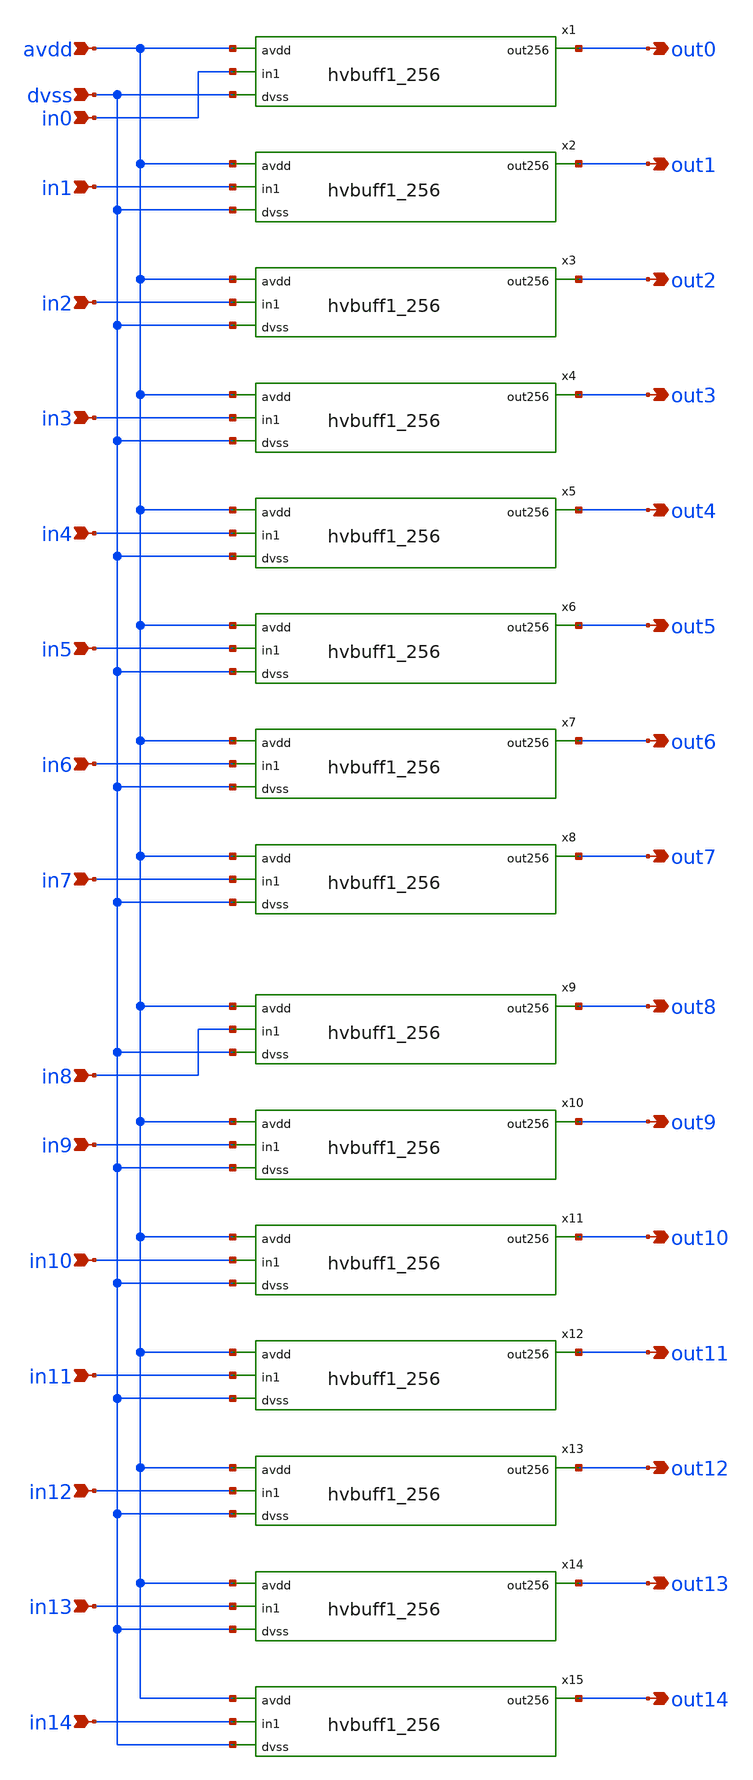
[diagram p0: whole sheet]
** sch_path: xschem/buff15ch.sch
**.subckt buff15ch out0 out1 out2 out3 out4 out5 out6 out7 in0 in1 in2 in3 in4 in5 in6 in7 out8 out9
*+ out10 out11 out12 out13 out14 in8 in9 in10 in11 in12 in13 in14 avdd dvss
*.opin out0
*.opin out1
*.opin out2
*.opin out3
*.opin out4
*.opin out5
*.opin out6
*.opin out7
*.ipin in0
*.ipin in1
*.ipin in2
*.ipin in3
*.ipin in4
*.ipin in5
*.ipin in6
*.ipin in7
*.opin out8
*.opin out9
*.opin out10
*.opin out11
*.opin out12
*.opin out13
*.opin out14
*.ipin in8
*.ipin in9
*.ipin in10
*.ipin in11
*.ipin in12
*.ipin in13
*.ipin in14
*.ipin avdd
*.ipin dvss
x1 avdd in0 out0 dvss hvbuff1_256
x2 avdd in1 out1 dvss hvbuff1_256
x3 avdd in2 out2 dvss hvbuff1_256
x4 avdd in3 out3 dvss hvbuff1_256
x5 avdd in4 out4 dvss hvbuff1_256
x6 avdd in5 out5 dvss hvbuff1_256
x7 avdd in6 out6 dvss hvbuff1_256
x8 avdd in7 out7 dvss hvbuff1_256
x9 avdd in8 out8 dvss hvbuff1_256
x10 avdd in9 out9 dvss hvbuff1_256
x11 avdd in10 out10 dvss hvbuff1_256
x12 avdd in11 out11 dvss hvbuff1_256
x13 avdd in12 out12 dvss hvbuff1_256
x14 avdd in13 out13 dvss hvbuff1_256
x15 avdd in14 out14 dvss hvbuff1_256
**.ends

* expanding   symbol:  hvbuff1_256.sym # of pins=4
** sym_path: xschem/hvbuff1_256.sym
** sch_path: xschem/hvbuff1_256.sch
.subckt hvbuff1_256 avdd in1 out256 dvss
*.ipin avdd
*.ipin in1
*.ipin dvss
*.opin out256
x2 net1 dvss dvss avdd avdd net2 sky130_fd_sc_hvl__inv_4
x1 net2 dvss dvss avdd avdd net3 sky130_fd_sc_hvl__inv_16
x3 net3 dvss dvss avdd avdd out256 sky130_fd_sc_hvl__inv_16
x4 net3 dvss dvss avdd avdd out256 sky130_fd_sc_hvl__inv_16
x5 net3 dvss dvss avdd avdd out256 sky130_fd_sc_hvl__inv_16
x6 net3 dvss dvss avdd avdd out256 sky130_fd_sc_hvl__inv_16
x7 in1 dvss dvss avdd avdd net1 sky130_fd_sc_hvl__inv_1
.ends

.end
